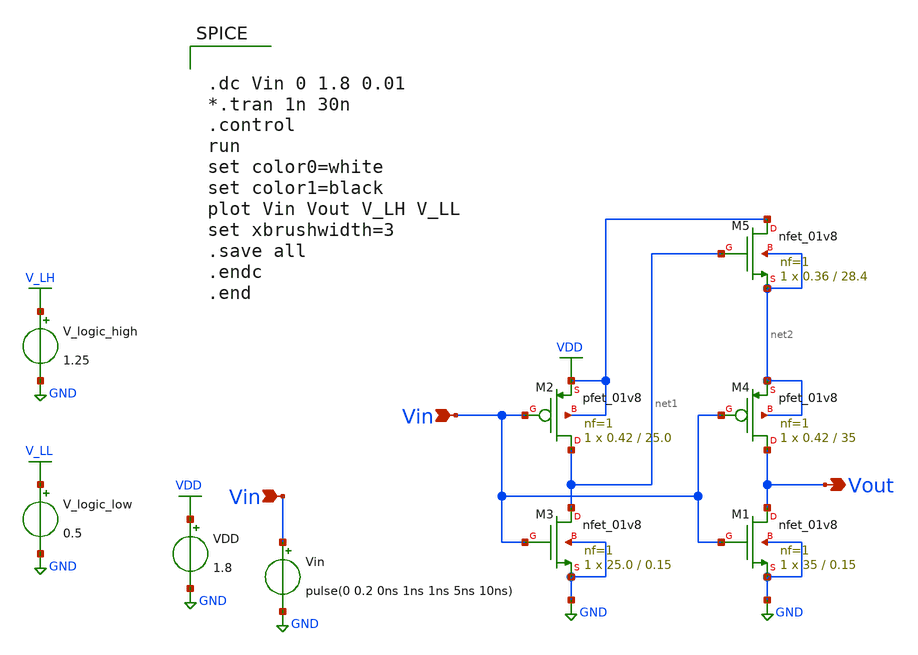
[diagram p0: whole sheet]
** sch_path: xschem/Vth_sch/Inverter-th3.sch
**.subckt Inverter-th3 Vin Vin Vout
*.ipin Vin
*.ipin Vin
*.opin Vout
VDD VDD GND 1.8
Vin Vin GND pulse(0 0.2 0ns 1ns 1ns 5ns 10ns)
V_logic_high V_LH GND 1.25
V_logic_low V_LL GND 0.5
XM3 net1 Vin GND GND sky130_fd_pr__nfet_01v8 L=0.15 W=25.0 nf=1 ad='int((nf+1)/2) * W/nf * 0.29' as='int((nf+2)/2) * W/nf * 0.29'
+ pd='2*int((nf+1)/2) * (W/nf + 0.29)' ps='2*int((nf+2)/2) * (W/nf + 0.29)' nrd='0.29 / W' nrs='0.29 / W'
+ sa=0 sb=0 sd=0 mult=1 m=1
XM2 net1 Vin VDD VDD sky130_fd_pr__pfet_01v8 L=25.0 W=0.42 nf=1 ad='int((nf+1)/2) * W/nf * 0.29' as='int((nf+2)/2) * W/nf * 0.29'
+ pd='2*int((nf+1)/2) * (W/nf + 0.29)' ps='2*int((nf+2)/2) * (W/nf + 0.29)' nrd='0.29 / W' nrs='0.29 / W'
+ sa=0 sb=0 sd=0 mult=1 m=1
XM1 Vout Vin GND GND sky130_fd_pr__nfet_01v8 L=0.15 W=35 nf=1 ad='int((nf+1)/2) * W/nf * 0.29' as='int((nf+2)/2) * W/nf * 0.29'
+ pd='2*int((nf+1)/2) * (W/nf + 0.29)' ps='2*int((nf+2)/2) * (W/nf + 0.29)' nrd='0.29 / W' nrs='0.29 / W'
+ sa=0 sb=0 sd=0 mult=1 m=1
XM4 Vout Vin net2 net2 sky130_fd_pr__pfet_01v8 L=35 W=0.42 nf=1 ad='int((nf+1)/2) * W/nf * 0.29' as='int((nf+2)/2) * W/nf * 0.29'
+ pd='2*int((nf+1)/2) * (W/nf + 0.29)' ps='2*int((nf+2)/2) * (W/nf + 0.29)' nrd='0.29 / W' nrs='0.29 / W'
+ sa=0 sb=0 sd=0 mult=1 m=1
XM5 VDD net1 net2 net2 sky130_fd_pr__nfet_01v8 L=28.4 W=0.36 nf=1 ad='int((nf+1)/2) * W/nf * 0.29' as='int((nf+2)/2) * W/nf * 0.29'
+ pd='2*int((nf+1)/2) * (W/nf + 0.29)' ps='2*int((nf+2)/2) * (W/nf + 0.29)' nrd='0.29 / W' nrs='0.29 / W'
+ sa=0 sb=0 sd=0 mult=1 m=1
**** begin user architecture code


.lib /usr/local/share/pdk/sky130A/libs.tech/ngspice/sky130.lib.spice tt

.save all





.dc Vin 0 1.8 0.01
*.tran 1n 30n
.control
run
set color0=white
set color1=black
plot Vin Vout V_LH V_LL
set xbrushwidth=3
.save all
.endc
.end


**** end user architecture code
**.ends
.GLOBAL VDD
.GLOBAL GND
.GLOBAL V_LH
.GLOBAL V_LL
.end
